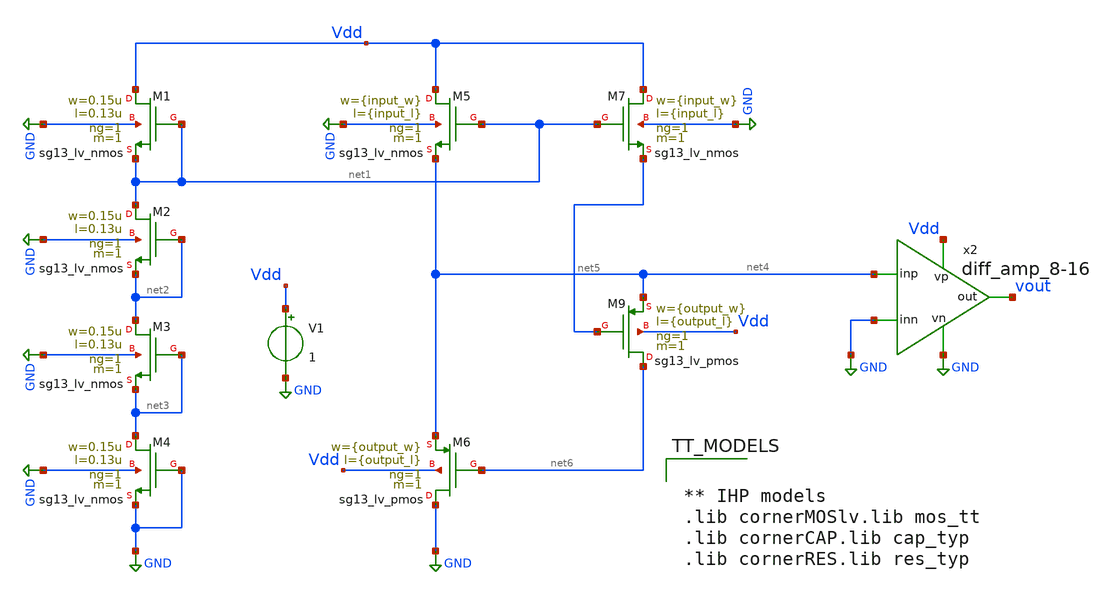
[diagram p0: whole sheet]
** sch_path: TempSensor/design_data/xschem/ptat_nmos_only_amp_tb.sch
**.subckt ptat_nmos_only_amp_tb
XM1 Vdd net1 net1 GND sg13_lv_nmos w=0.15u l=0.13u ng=1 m=1 mm_ok=1
XM2 net1 net2 net2 GND sg13_lv_nmos w=0.15u l=0.13u ng=1 m=1 mm_ok=1
XM3 net2 net3 net3 GND sg13_lv_nmos w=0.15u l=0.13u ng=1 m=1 mm_ok=1
XM4 net3 GND GND GND sg13_lv_nmos w=0.15u l=0.13u ng=1 m=1 mm_ok=1
XM5 Vdd net1 net4 GND sg13_lv_nmos w={input_w} l={input_l} ng=1 m=1 mm_ok=1
XM7 Vdd net1 net5 GND sg13_lv_nmos w={input_w} l={input_l} ng=1 m=1 mm_ok=1
V1 Vdd GND 1
XM9 net6 net5 net4 Vdd sg13_lv_pmos w={output_w} l={output_l} ng=1 m=1 mm_ok=1
XM6 GND net6 net4 Vdd sg13_lv_pmos w={output_w} l={output_l} ng=1 m=1 mm_ok=1
x2 Vdd GND net4 vout GND diff_amp_8-16
**** begin user architecture code


.param input_w = 0.1u input_l = 0.33u
.param output_w = 0.15u output_l = 0.33u
.control
*shell rm DELETE_ME_ptat_nmos_only.csv ptat_nmos_only.raw
unlet all.vout
save all

set wr_singlescale            ; for wrdata: write the scale only once
set wr_vecnames               ; for wrdata: write the vector names

foreach wval 0.1u 0.5u 1u 2u 5u
 alterparam input_w = $wval
 echo '=== wval = $wval'
 echo '=== curplot = $curplot'
 reset
 dc temp 0 125 1
end

*wrdata DELETE_ME_ptat_nmos_only.csv all.vout
write $inputdir/ptat_nmos_only_varinpw_amp.raw all.vout
*plot all.vout
.endc




** IHP models
.lib cornerMOSlv.lib mos_tt
.lib cornerCAP.lib cap_typ
.lib cornerRES.lib res_typ


**** end user architecture code
**.ends

* expanding   symbol:  practicing/TempSensor/design_data/xschem/diff_amp_8-16.sym # of pins=5
** sym_path: TempSensor/design_data/xschem/diff_amp_8-16.sym
** sch_path: TempSensor/design_data/xschem/diff_amp_8-16.sch
.subckt diff_amp_8-16 vp inn inp out vn
*.ipin inp
*.opin out
*.ipin inn
*.iopin vn
*.iopin vp
XM6 net10 inn net2 vn sg13_lv_nmos w=10u l=0.5u ng=1 m=1 mm_ok=1
XM5 net11 inp net2 vn sg13_lv_nmos w=10u l=0.5u ng=1 m=1 mm_ok=1
XM2 net1 net1 net4 vp sg13_lv_pmos w=10u l=2u ng=1 m=10 mm_ok=1
XM1 net4 net1 vp vp sg13_lv_pmos w=6u l=1u ng=1 m=1 mm_ok=1
XM3 net3 net1 vp vp sg13_lv_pmos w=6u l=1u ng=1 m=1 mm_ok=1
XM4 net5 net1 net3 vp sg13_lv_pmos w=10u l=2u ng=1 m=10 mm_ok=1
XM7 net5 net5 net6 vn sg13_lv_nmos w=10u l=2u ng=1 m=10 mm_ok=1
XM8 net6 net5 vn vn sg13_lv_nmos w=10u l=5u ng=1 m=1 mm_ok=1
XM9 net2 net5 net7 vn sg13_lv_nmos w=10u l=2u ng=1 m=10 mm_ok=1
XM10 net7 net5 vn vn sg13_lv_nmos w=10u l=5u ng=1 m=1 mm_ok=1
XM15 net8 net8 vn vn sg13_lv_nmos w=10u l=1.5u ng=1 m=1 mm_ok=1
XM16 net9 net8 vn vn sg13_lv_nmos w=10u l=1.5u ng=1 m=1 mm_ok=1
XM11 net10 net1 vp vp sg13_lv_pmos w=10u l=1.67u ng=1 m=1 mm_ok=1
XM12 net8 net1 net10 vp sg13_lv_pmos w=10u l=2u ng=1 m=10 mm_ok=1
XM13 net11 net1 vp vp sg13_lv_pmos w=10u l=1.67u ng=1 m=1 mm_ok=1
XM14 net9 net1 net11 vp sg13_lv_pmos w=10u l=2u ng=1 m=10 mm_ok=1
XM17 out net1 vp vp sg13_lv_pmos w=9u l=5u ng=1 m=10 mm_ok=1
XM18 out net9 vn vn sg13_lv_nmos w=10u l=0.5u ng=1 m=5 mm_ok=1
I0 net1 vn 20u
XC2 out net9 cap_cmim w=35e-6 l=35e-6 m=1 mm_ok=1
.ends

.GLOBAL GND
.end
